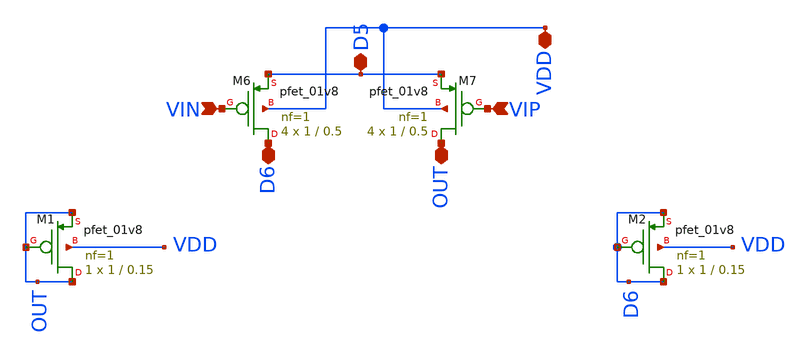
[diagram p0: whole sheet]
** sch_path: pmoscs2.sch
**.subckt pmoscs2 VIN VIP OUT D6 VDD D5
*.ipin VIN
*.ipin VIP
*.iopin OUT
*.iopin D6
*.iopin VDD
*.iopin D5
XM6 D6 VIN D5 VDD sky130_fd_pr__pfet_01v8 L=0.5 W=1 nf=1 ad='int((nf+1)/2) * W/nf * 0.29' as='int((nf+2)/2) * W/nf * 0.29'
+ pd='2*int((nf+1)/2) * (W/nf + 0.29)' ps='2*int((nf+2)/2) * (W/nf + 0.29)' nrd='0.29 / W' nrs='0.29 / W'
+ sa=0 sb=0 sd=0 mult=4 m=4
XM7 OUT VIP D5 VDD sky130_fd_pr__pfet_01v8 L=0.5 W=1 nf=1 ad='int((nf+1)/2) * W/nf * 0.29' as='int((nf+2)/2) * W/nf * 0.29'
+ pd='2*int((nf+1)/2) * (W/nf + 0.29)' ps='2*int((nf+2)/2) * (W/nf + 0.29)' nrd='0.29 / W' nrs='0.29 / W'
+ sa=0 sb=0 sd=0 mult=4 m=4
XM1 OUT OUT OUT VDD sky130_fd_pr__pfet_01v8 L=0.15 W=1 nf=1 ad='int((nf+1)/2) * W/nf * 0.29' as='int((nf+2)/2) * W/nf * 0.29'
+ pd='2*int((nf+1)/2) * (W/nf + 0.29)' ps='2*int((nf+2)/2) * (W/nf + 0.29)' nrd='0.29 / W' nrs='0.29 / W'
+ sa=0 sb=0 sd=0 mult=1 m=1
XM2 D6 D6 D6 VDD sky130_fd_pr__pfet_01v8 L=0.15 W=1 nf=1 ad='int((nf+1)/2) * W/nf * 0.29' as='int((nf+2)/2) * W/nf * 0.29'
+ pd='2*int((nf+1)/2) * (W/nf + 0.29)' ps='2*int((nf+2)/2) * (W/nf + 0.29)' nrd='0.29 / W' nrs='0.29 / W'
+ sa=0 sb=0 sd=0 mult=1 m=1
**.ends
.end
